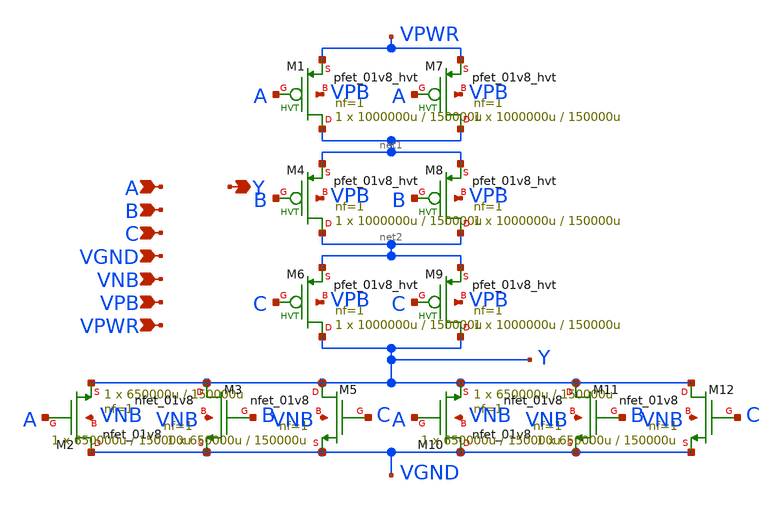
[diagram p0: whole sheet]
** sch_path: schematics/nor3/sky130_fd_sc_hd__nor3_2.sch
**.subckt sky130_fd_sc_hd__nor3_2 A B C VGND VNB VPB VPWR Y
*.ipin A
*.ipin B
*.ipin C
*.ipin VGND
*.ipin VNB
*.ipin VPB
*.ipin VPWR
*.opin Y
XM1 net1 A VPWR VPB sky130_fd_pr__pfet_01v8_hvt L=150000u W=1000000u nf=1 ad='int((1 + 1)/2) * 1000000u / 1 * 0.29'
+ as='int((1 + 2)/2) * 1000000u / 1 * 0.29' pd='2*int((1 + 1)/2) * (1000000u / 1 + 0.29)' ps='2*int((1 + 2)/2) * (1000000u / 1 + 0.29)'
+ nrd='0.29 / 1000000u ' nrs='0.29 / 1000000u ' sa=0 sb=0 sd=0 mult=1 m=1
XM2 VGND A Y VNB sky130_fd_pr__nfet_01v8 L=150000u W=650000u nf=1 ad='int((1 + 1)/2) * 650000u / 1 * 0.29'
+ as='int((1 + 2)/2) * 650000u / 1 * 0.29' pd='2*int((1 + 1)/2) * (650000u / 1 + 0.29)' ps='2*int((1 + 2)/2) * (650000u / 1 + 0.29)'
+ nrd='0.29 / 650000u ' nrs='0.29 / 650000u ' sa=0 sb=0 sd=0 mult=1 m=1
XM4 net2 B net1 VPB sky130_fd_pr__pfet_01v8_hvt L=150000u W=1000000u nf=1 ad='int((1 + 1)/2) * 1000000u / 1 * 0.29'
+ as='int((1 + 2)/2) * 1000000u / 1 * 0.29' pd='2*int((1 + 1)/2) * (1000000u / 1 + 0.29)' ps='2*int((1 + 2)/2) * (1000000u / 1 + 0.29)'
+ nrd='0.29 / 1000000u ' nrs='0.29 / 1000000u ' sa=0 sb=0 sd=0 mult=1 m=1
XM3 Y B VGND VNB sky130_fd_pr__nfet_01v8 L=150000u W=650000u nf=1 ad='int((1 + 1)/2) * 650000u / 1 * 0.29'
+ as='int((1 + 2)/2) * 650000u / 1 * 0.29' pd='2*int((1 + 1)/2) * (650000u / 1 + 0.29)' ps='2*int((1 + 2)/2) * (650000u / 1 + 0.29)'
+ nrd='0.29 / 650000u ' nrs='0.29 / 650000u ' sa=0 sb=0 sd=0 mult=1 m=1
XM5 Y C VGND VNB sky130_fd_pr__nfet_01v8 L=150000u W=650000u nf=1 ad='int((1 + 1)/2) * 650000u / 1 * 0.29'
+ as='int((1 + 2)/2) * 650000u / 1 * 0.29' pd='2*int((1 + 1)/2) * (650000u / 1 + 0.29)' ps='2*int((1 + 2)/2) * (650000u / 1 + 0.29)'
+ nrd='0.29 / 650000u ' nrs='0.29 / 650000u ' sa=0 sb=0 sd=0 mult=1 m=1
XM6 Y C net2 VPB sky130_fd_pr__pfet_01v8_hvt L=150000u W=1000000u nf=1 ad='int((1 + 1)/2) * 1000000u / 1 * 0.29'
+ as='int((1 + 2)/2) * 1000000u / 1 * 0.29' pd='2*int((1 + 1)/2) * (1000000u / 1 + 0.29)' ps='2*int((1 + 2)/2) * (1000000u / 1 + 0.29)'
+ nrd='0.29 / 1000000u ' nrs='0.29 / 1000000u ' sa=0 sb=0 sd=0 mult=1 m=1
XM7 net1 A VPWR VPB sky130_fd_pr__pfet_01v8_hvt L=150000u W=1000000u nf=1 ad='int((1 + 1)/2) * 1000000u / 1 * 0.29'
+ as='int((1 + 2)/2) * 1000000u / 1 * 0.29' pd='2*int((1 + 1)/2) * (1000000u / 1 + 0.29)' ps='2*int((1 + 2)/2) * (1000000u / 1 + 0.29)'
+ nrd='0.29 / 1000000u ' nrs='0.29 / 1000000u ' sa=0 sb=0 sd=0 mult=1 m=1
XM8 net2 B net1 VPB sky130_fd_pr__pfet_01v8_hvt L=150000u W=1000000u nf=1 ad='int((1 + 1)/2) * 1000000u / 1 * 0.29'
+ as='int((1 + 2)/2) * 1000000u / 1 * 0.29' pd='2*int((1 + 1)/2) * (1000000u / 1 + 0.29)' ps='2*int((1 + 2)/2) * (1000000u / 1 + 0.29)'
+ nrd='0.29 / 1000000u ' nrs='0.29 / 1000000u ' sa=0 sb=0 sd=0 mult=1 m=1
XM9 Y C net2 VPB sky130_fd_pr__pfet_01v8_hvt L=150000u W=1000000u nf=1 ad='int((1 + 1)/2) * 1000000u / 1 * 0.29'
+ as='int((1 + 2)/2) * 1000000u / 1 * 0.29' pd='2*int((1 + 1)/2) * (1000000u / 1 + 0.29)' ps='2*int((1 + 2)/2) * (1000000u / 1 + 0.29)'
+ nrd='0.29 / 1000000u ' nrs='0.29 / 1000000u ' sa=0 sb=0 sd=0 mult=1 m=1
XM10 VGND A Y VNB sky130_fd_pr__nfet_01v8 L=150000u W=650000u nf=1 ad='int((1 + 1)/2) * 650000u / 1 * 0.29'
+ as='int((1 + 2)/2) * 650000u / 1 * 0.29' pd='2*int((1 + 1)/2) * (650000u / 1 + 0.29)' ps='2*int((1 + 2)/2) * (650000u / 1 + 0.29)'
+ nrd='0.29 / 650000u ' nrs='0.29 / 650000u ' sa=0 sb=0 sd=0 mult=1 m=1
XM11 Y B VGND VNB sky130_fd_pr__nfet_01v8 L=150000u W=650000u nf=1 ad='int((1 + 1)/2) * 650000u / 1 * 0.29'
+ as='int((1 + 2)/2) * 650000u / 1 * 0.29' pd='2*int((1 + 1)/2) * (650000u / 1 + 0.29)' ps='2*int((1 + 2)/2) * (650000u / 1 + 0.29)'
+ nrd='0.29 / 650000u ' nrs='0.29 / 650000u ' sa=0 sb=0 sd=0 mult=1 m=1
XM12 Y C VGND VNB sky130_fd_pr__nfet_01v8 L=150000u W=650000u nf=1 ad='int((1 + 1)/2) * 650000u / 1 * 0.29'
+ as='int((1 + 2)/2) * 650000u / 1 * 0.29' pd='2*int((1 + 1)/2) * (650000u / 1 + 0.29)' ps='2*int((1 + 2)/2) * (650000u / 1 + 0.29)'
+ nrd='0.29 / 650000u ' nrs='0.29 / 650000u ' sa=0 sb=0 sd=0 mult=1 m=1
**.ends
.end
